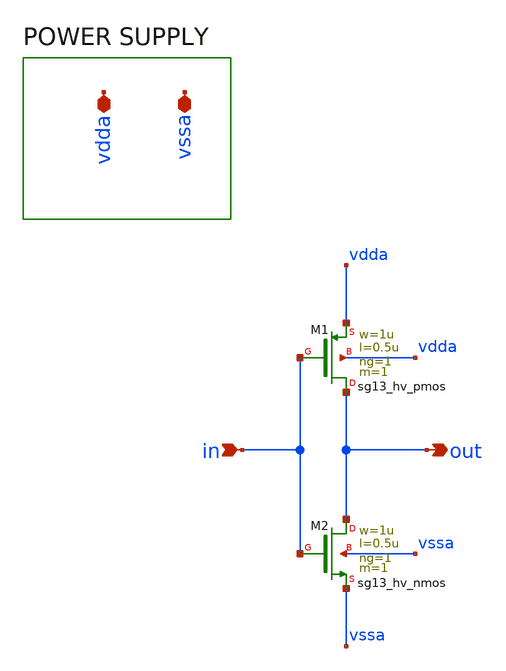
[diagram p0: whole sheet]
** sch_path: inv.sch
**.subckt inv in out vssa vdda
*.ipin in
*.opin out
*.iopin vssa
*.iopin vdda
XM1 out in vdda vdda sg13_hv_pmos w=1u l=0.5u ng=1 m=1 mm_ok=1
XM2 out in vssa vssa sg13_hv_nmos w=1u l=0.5u ng=1 m=1 mm_ok=1
**.ends
.end
